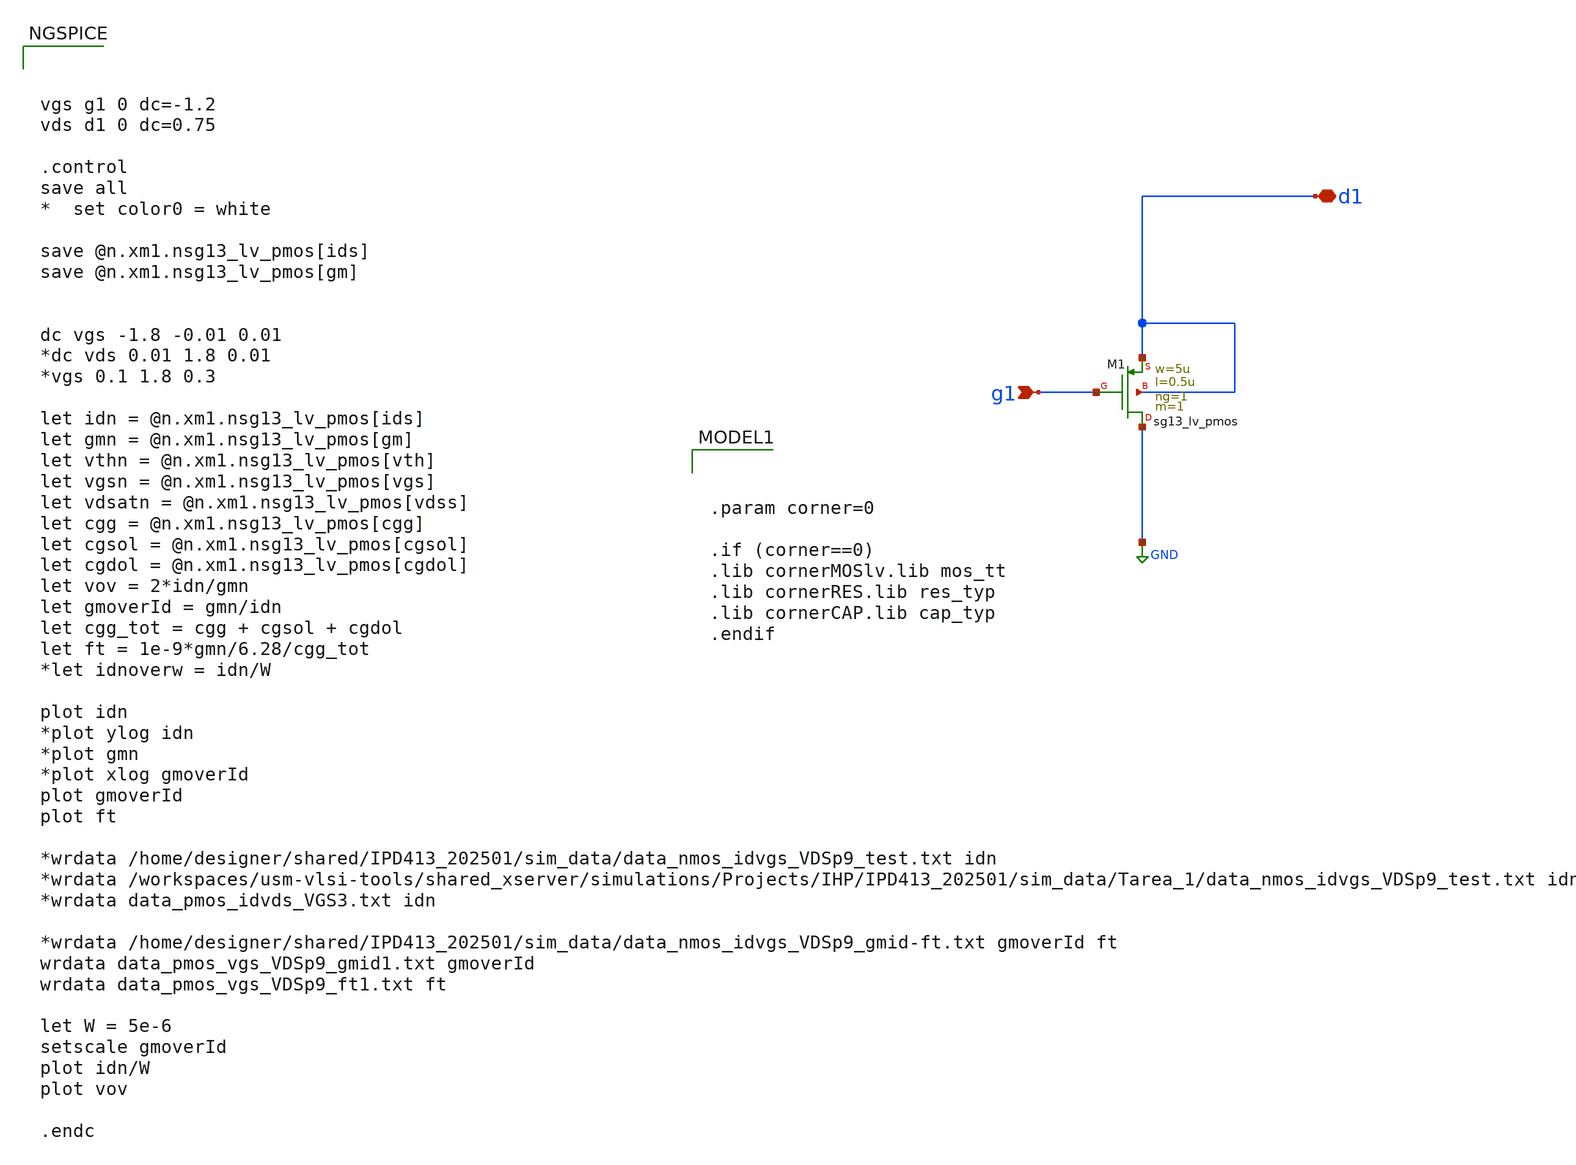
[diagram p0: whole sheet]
** sch_path: others/single mos/tb_pmoslv_charac.sch
**.subckt tb_pmoslv_charac g1 d1
*.ipin g1
*.iopin d1
XM1 GND g1 d1 d1 sg13_lv_pmos w=5u l=0.5u ng=1 m=1 mm_ok=1
**** begin user architecture code



vgs g1 0 dc=-1.2
vds d1 0 dc=0.75

.control
save all
*  set color0 = white

save @n.xm1.nsg13_lv_pmos[ids]
save @n.xm1.nsg13_lv_pmos[gm]


dc vgs -1.8 -0.01 0.01
*dc vds 0.01 1.8 0.01
*vgs 0.1 1.8 0.3

let idn = @n.xm1.nsg13_lv_pmos[ids]
let gmn = @n.xm1.nsg13_lv_pmos[gm]
let vthn = @n.xm1.nsg13_lv_pmos[vth]
let vgsn = @n.xm1.nsg13_lv_pmos[vgs]
let vdsatn = @n.xm1.nsg13_lv_pmos[vdss]
let cgg = @n.xm1.nsg13_lv_pmos[cgg]
let cgsol = @n.xm1.nsg13_lv_pmos[cgsol]
let cgdol = @n.xm1.nsg13_lv_pmos[cgdol]
let vov = 2*idn/gmn
let gmoverId = gmn/idn
let cgg_tot = cgg + cgsol + cgdol
let ft = 1e-9*gmn/6.28/cgg_tot
*let idnoverw = idn/W

plot idn
*plot ylog idn
*plot gmn
*plot xlog gmoverId
plot gmoverId
plot ft

*wrdata /home/designer/shared/IPD413_202501/sim_data/data_nmos_idvgs_VDSp9_test.txt idn
*wrdata
*+ /workspaces/usm-vlsi-tools/shared_xserver/simulations/Projects/IHP/IPD413_202501/sim_data/Tarea_1/data_nmos_idvgs_VDSp9_test.txt idn
*wrdata data_pmos_idvds_VGS3.txt idn

*wrdata /home/designer/shared/IPD413_202501/sim_data/data_nmos_idvgs_VDSp9_gmid-ft.txt gmoverId ft
wrdata data_pmos_vgs_VDSp9_gmid1.txt gmoverId
wrdata data_pmos_vgs_VDSp9_ft1.txt ft

let W = 5e-6
setscale gmoverId
plot idn/W
plot vov

.endc




.param corner=0

.if (corner==0)
.lib cornerMOSlv.lib mos_tt
.lib cornerRES.lib res_typ
.lib cornerCAP.lib cap_typ
.endif

**** end user architecture code
**.ends
.GLOBAL GND
.end
